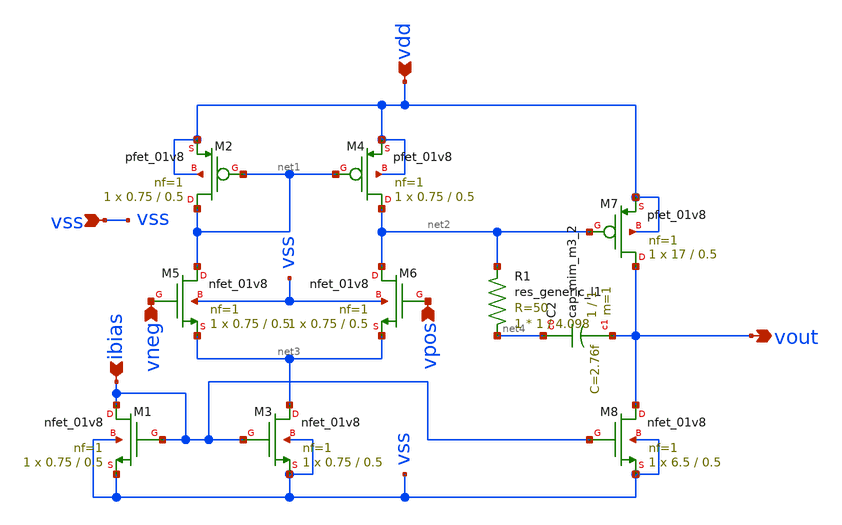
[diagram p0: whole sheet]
** sch_path: sch/opamp.sch
**.subckt opamp ibias vdd vneg vpos vss vout
*.ipin ibias
*.ipin vdd
*.ipin vneg
*.ipin vpos
*.ipin vss
*.opin vout
XM1 ibias ibias vss vss sky130_fd_pr__nfet_01v8 L=0.5 W=0.75 nf=1 ad='int((1 + 1)/2) * 0.75 / 1 * 0.29'
+ as='int((1 + 2)/2) * 0.75 / 1 * 0.29' pd='2*int((1 + 1)/2) * (0.75 / 1 + 0.29)' ps='2*int((1 + 2)/2) * (0.75 / 1 + 0.29)'
+ nrd='0.29 / 0.75 ' nrs='0.29 / 0.75 ' sa=0 sb=0 sd=0 mult=1 m=1
XM2 net1 net1 vdd vdd sky130_fd_pr__pfet_01v8 L=0.5 W=0.75 nf=1 ad='int((1 + 1)/2) * 0.75 / 1 * 0.29'
+ as='int((1 + 2)/2) * 0.75 / 1 * 0.29' pd='2*int((1 + 1)/2) * (0.75 / 1 + 0.29)' ps='2*int((1 + 2)/2) * (0.75 / 1 + 0.29)'
+ nrd='0.29 / 0.75 ' nrs='0.29 / 0.75 ' sa=0 sb=0 sd=0 mult=1 m=1
XM3 net3 ibias vss vss sky130_fd_pr__nfet_01v8 L=0.5 W=0.75 nf=1 ad='int((1 + 1)/2) * 0.75 / 1 * 0.29'
+ as='int((1 + 2)/2) * 0.75 / 1 * 0.29' pd='2*int((1 + 1)/2) * (0.75 / 1 + 0.29)' ps='2*int((1 + 2)/2) * (0.75 / 1 + 0.29)'
+ nrd='0.29 / 0.75 ' nrs='0.29 / 0.75 ' sa=0 sb=0 sd=0 mult=1 m=1
XM4 net2 net1 vdd vdd sky130_fd_pr__pfet_01v8 L=0.5 W=0.75 nf=1 ad='int((1 + 1)/2) * 0.75 / 1 * 0.29'
+ as='int((1 + 2)/2) * 0.75 / 1 * 0.29' pd='2*int((1 + 1)/2) * (0.75 / 1 + 0.29)' ps='2*int((1 + 2)/2) * (0.75 / 1 + 0.29)'
+ nrd='0.29 / 0.75 ' nrs='0.29 / 0.75 ' sa=0 sb=0 sd=0 mult=1 m=1
XM5 net1 vneg net3 vss sky130_fd_pr__nfet_01v8 L=0.5 W=0.75 nf=1 ad='int((1 + 1)/2) * 0.75 / 1 * 0.29'
+ as='int((1 + 2)/2) * 0.75 / 1 * 0.29' pd='2*int((1 + 1)/2) * (0.75 / 1 + 0.29)' ps='2*int((1 + 2)/2) * (0.75 / 1 + 0.29)'
+ nrd='0.29 / 0.75 ' nrs='0.29 / 0.75 ' sa=0 sb=0 sd=0 mult=1 m=1
XM6 net2 vpos net3 vss sky130_fd_pr__nfet_01v8 L=0.5 W=0.75 nf=1 ad='int((1 + 1)/2) * 0.75 / 1 * 0.29'
+ as='int((1 + 2)/2) * 0.75 / 1 * 0.29' pd='2*int((1 + 1)/2) * (0.75 / 1 + 0.29)' ps='2*int((1 + 2)/2) * (0.75 / 1 + 0.29)'
+ nrd='0.29 / 0.75 ' nrs='0.29 / 0.75 ' sa=0 sb=0 sd=0 mult=1 m=1
XM7 vout net2 vdd vdd sky130_fd_pr__pfet_01v8 L=0.5 W=17 nf=1 ad='int((1 + 1)/2) * 17 / 1 * 0.29' as='int((1 + 2)/2) * 17 / 1 * 0.29'
+ pd='2*int((1 + 1)/2) * (17 / 1 + 0.29)' ps='2*int((1 + 2)/2) * (17 / 1 + 0.29)' nrd='0.29 / 17 ' nrs='0.29 / 17 '
+ sa=0 sb=0 sd=0 mult=1 m=1
XM8 vout ibias vss vss sky130_fd_pr__nfet_01v8 L=0.5 W=6.5 nf=1 ad='int((1 + 1)/2) * 6.5 / 1 * 0.29'
+ as='int((1 + 2)/2) * 6.5 / 1 * 0.29' pd='2*int((1 + 1)/2) * (6.5 / 1 + 0.29)' ps='2*int((1 + 2)/2) * (6.5 / 1 + 0.29)'
+ nrd='0.29 / 6.5 ' nrs='0.29 / 6.5 ' sa=0 sb=0 sd=0 mult=1 m=1
XC2 net4 vout sky130_fd_pr__cap_mim_m3_2 W=1 L=1 MF=1 m=1
R1 net4 net2 sky130_fd_pr__res_generic_l1 W=1 L=4.098 m=1
**.ends
.end
